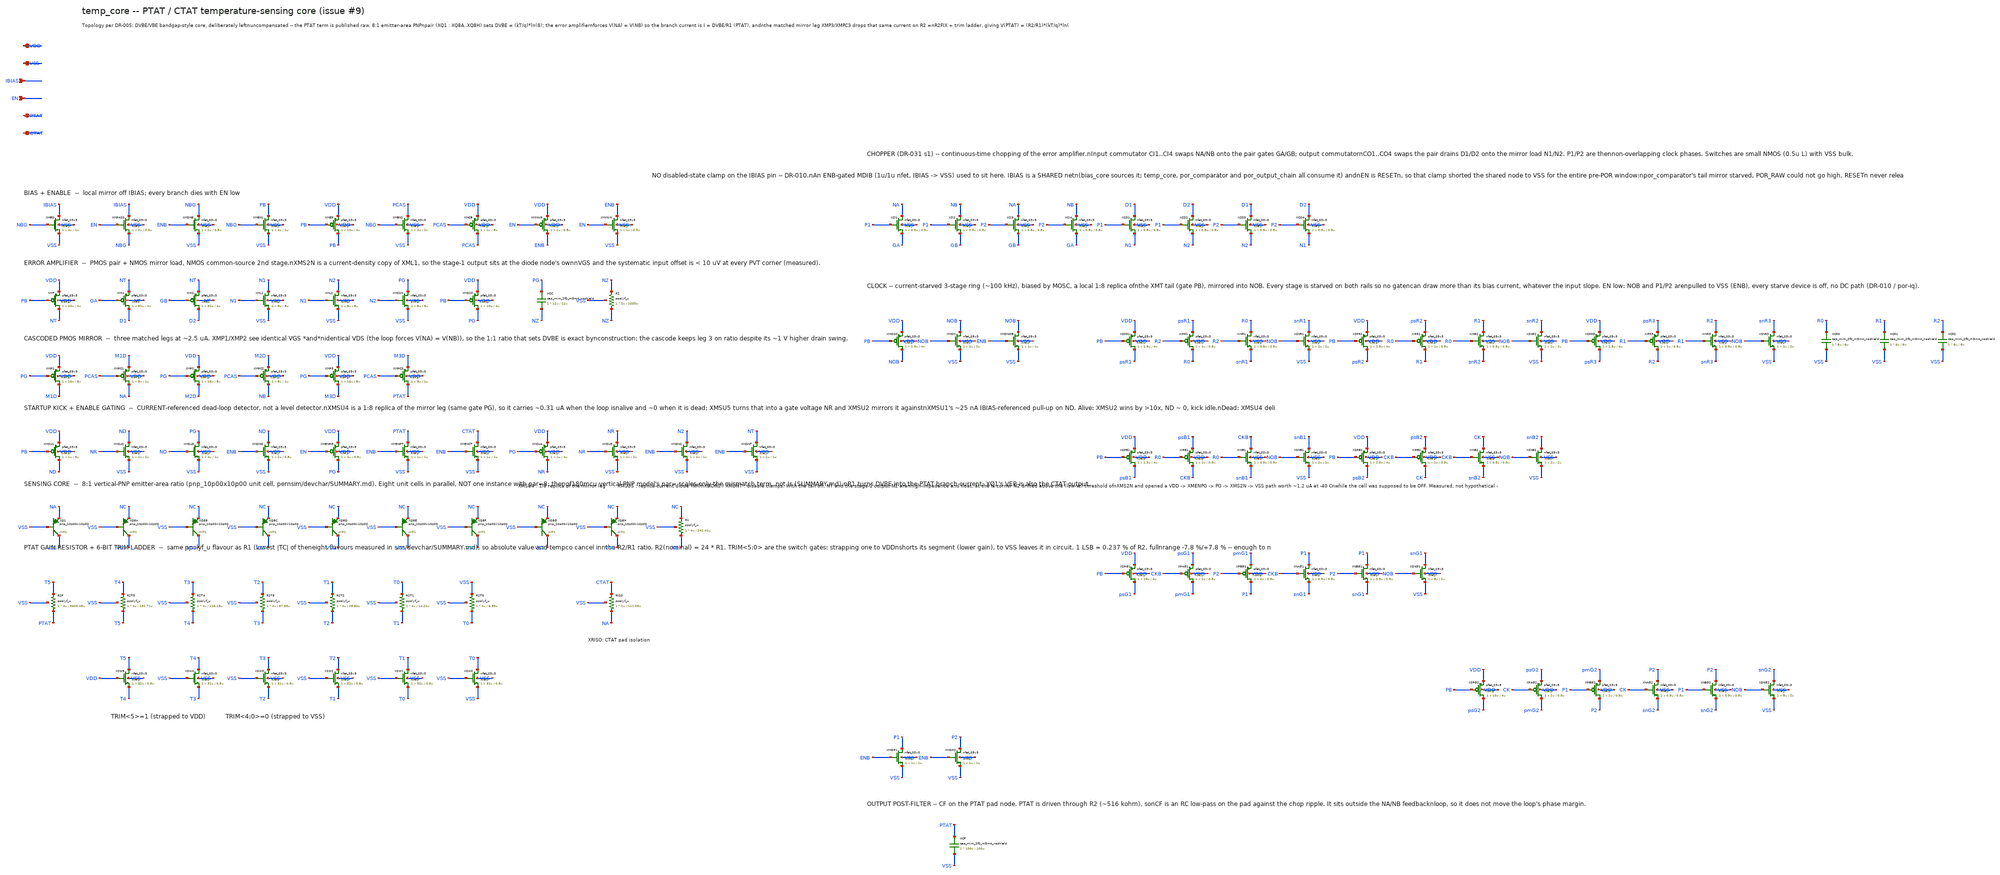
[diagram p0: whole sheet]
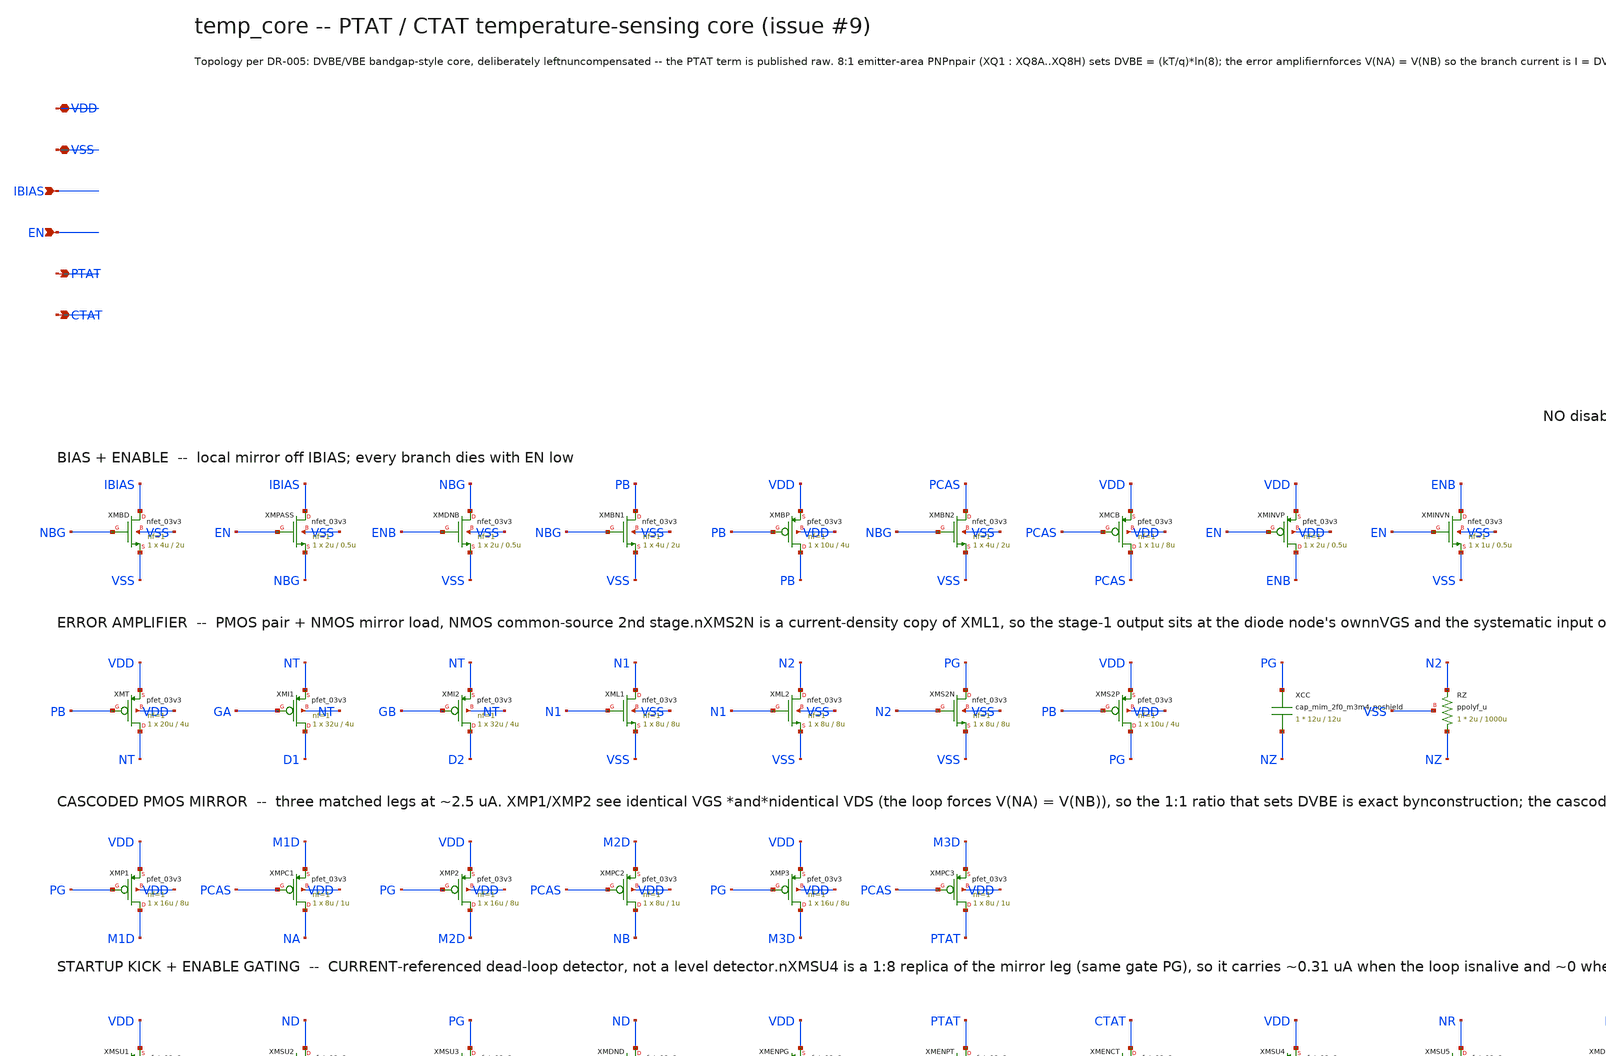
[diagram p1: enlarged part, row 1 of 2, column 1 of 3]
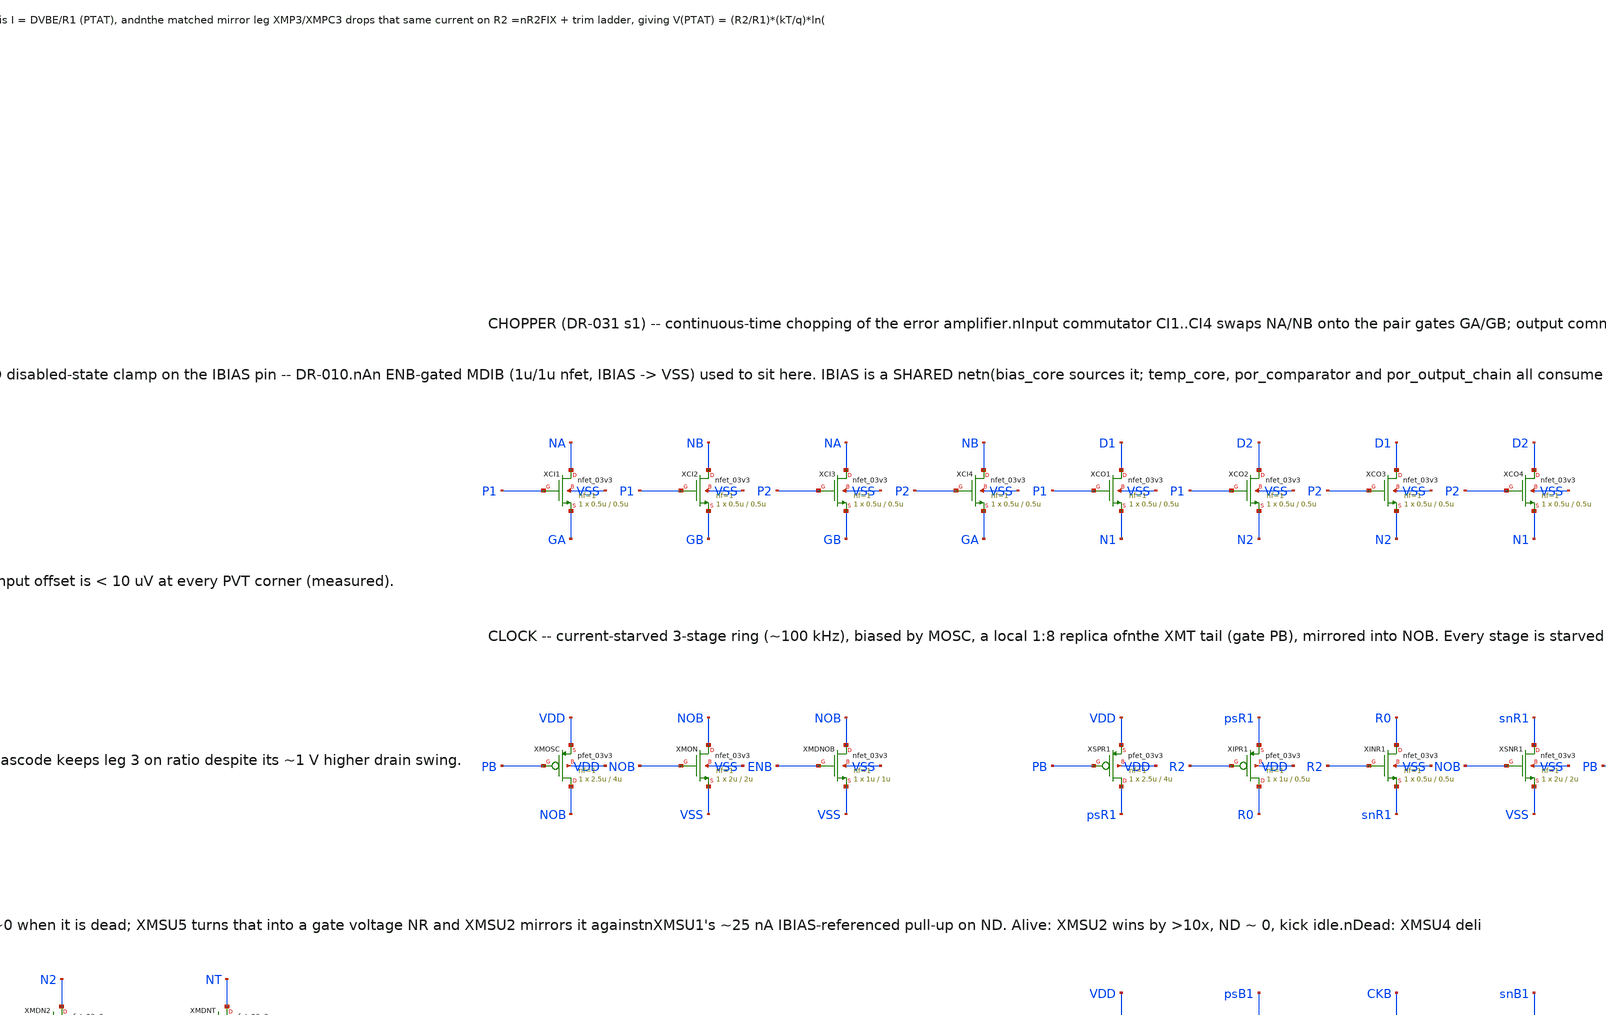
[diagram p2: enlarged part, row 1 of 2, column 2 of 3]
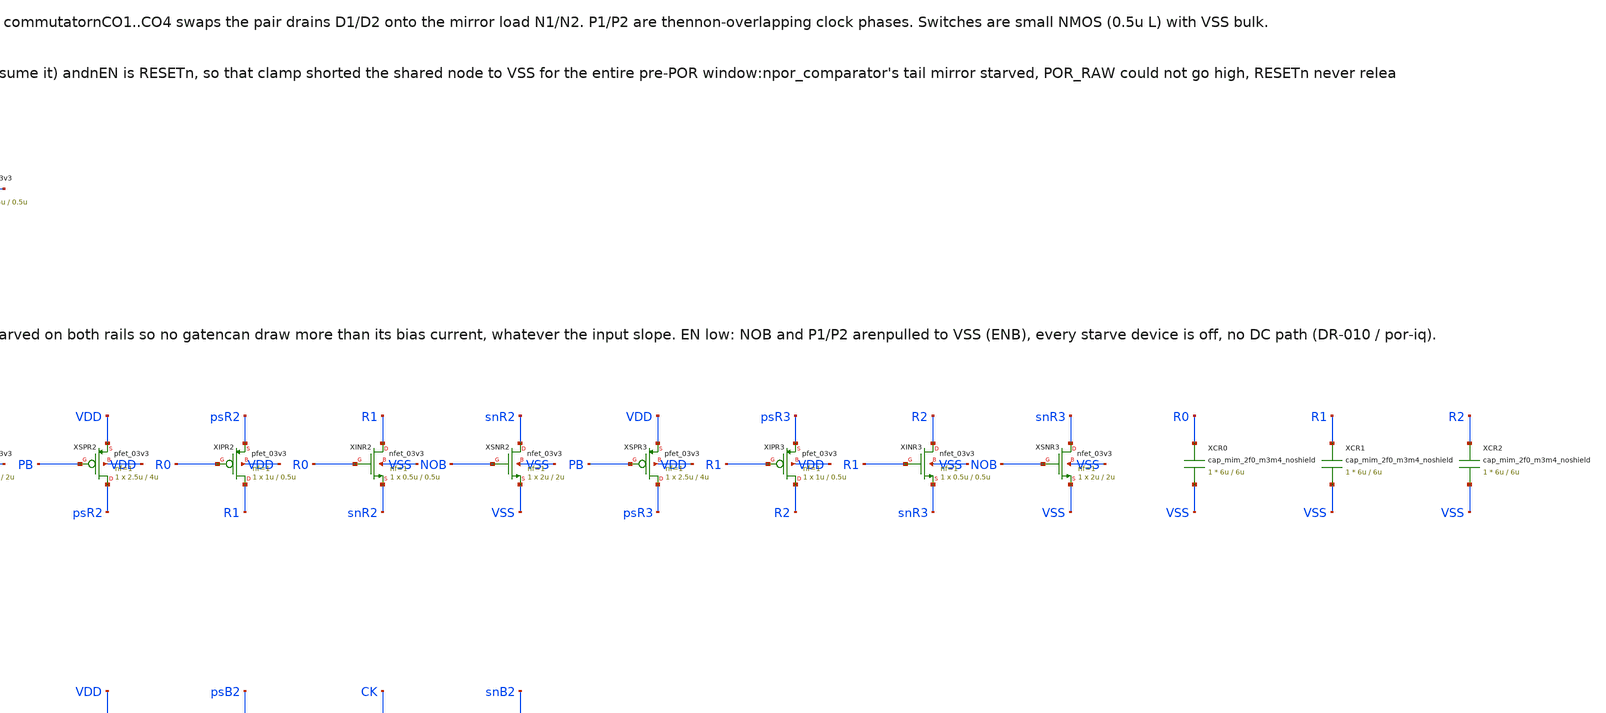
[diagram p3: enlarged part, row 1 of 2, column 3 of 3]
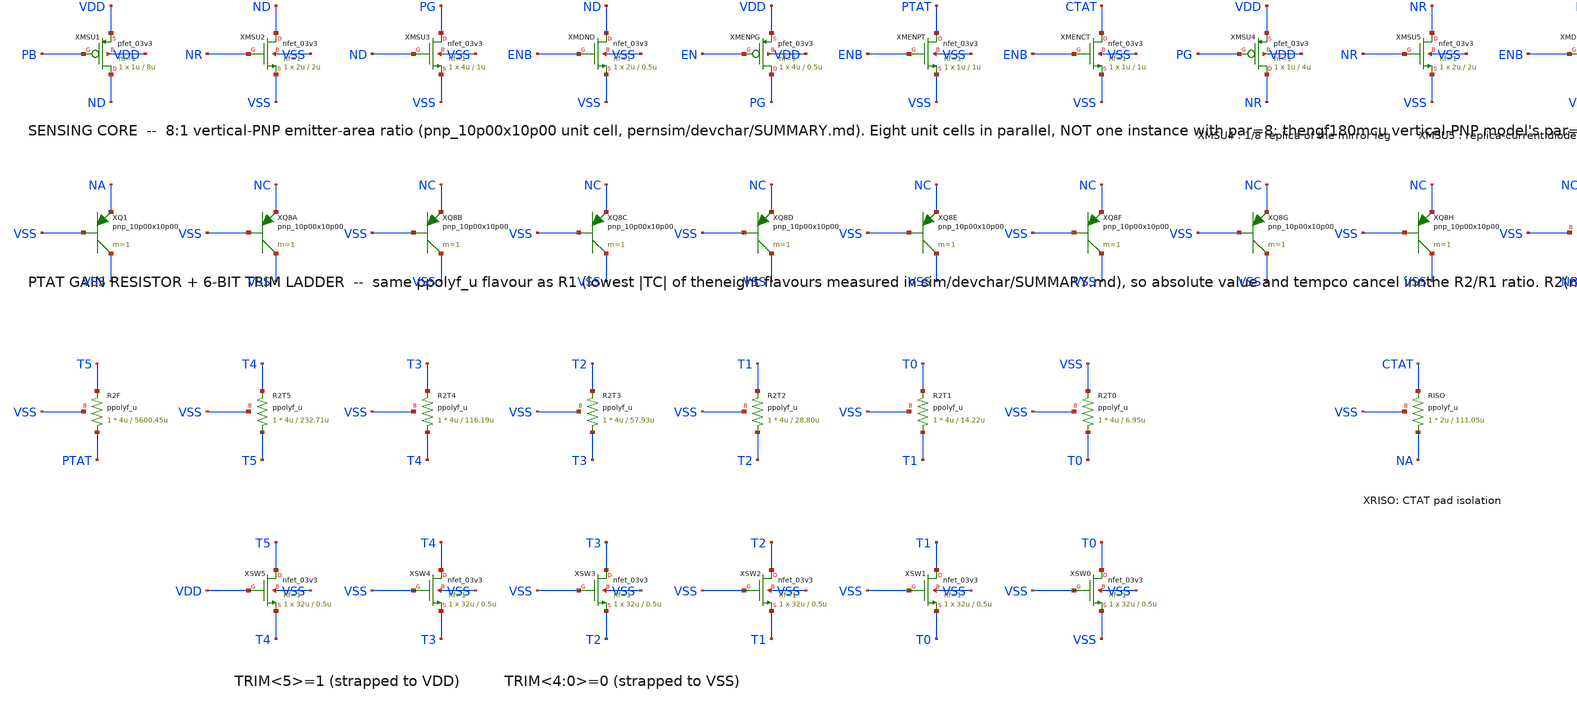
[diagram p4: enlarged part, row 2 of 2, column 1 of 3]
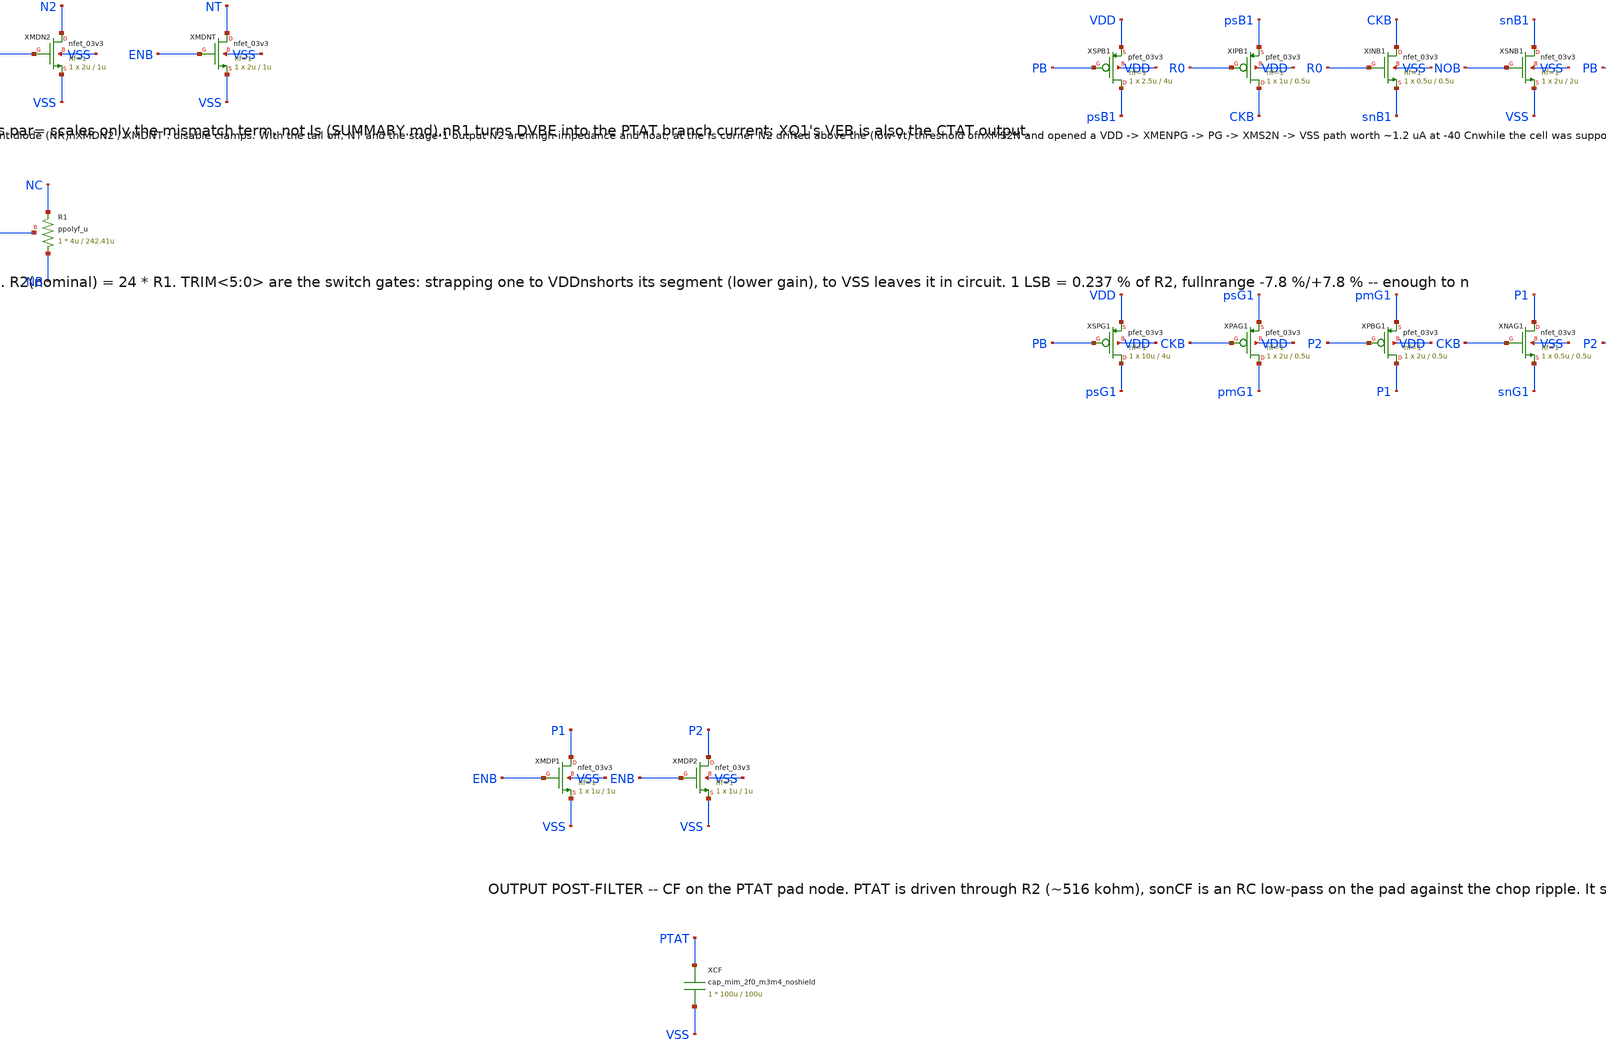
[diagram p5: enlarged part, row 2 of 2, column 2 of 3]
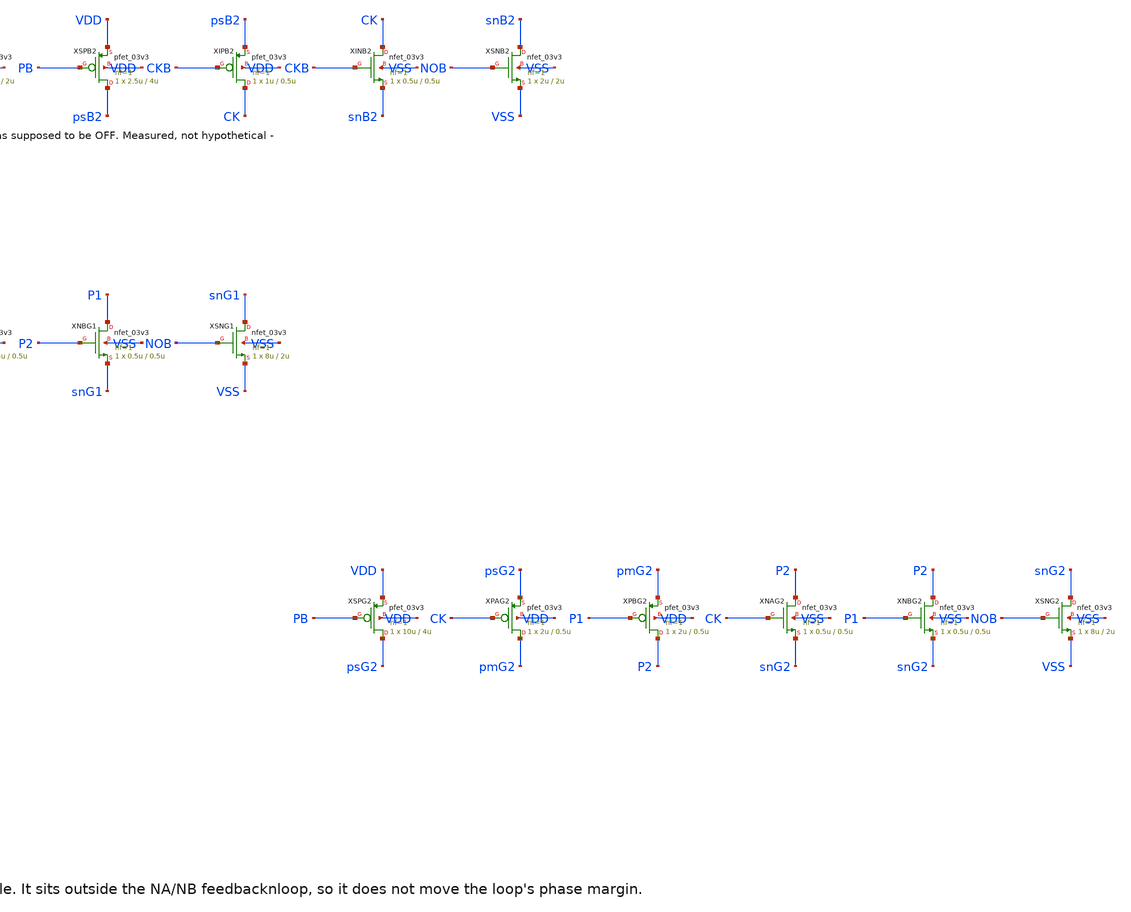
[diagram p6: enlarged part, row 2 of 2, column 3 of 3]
** sch_path: design/temp_core.sch
**.subckt temp_core VDD VSS IBIAS EN PTAT CTAT
*.iopin VDD
*.iopin VSS
*.ipin IBIAS
*.ipin EN
*.opin PTAT
*.opin CTAT
XMBD IBIAS NBG VSS VSS nfet_03v3 L=2u W=4u nf=1 ad='int((nf+1)/2) * W/nf * 0.18u' as='int((nf+2)/2) * W/nf * 0.18u'
+ pd='2*int((nf+1)/2) * (W/nf + 0.18u)' ps='2*int((nf+2)/2) * (W/nf + 0.18u)' nrd='0.18u / W' nrs='0.18u / W'
+ sa=0 sb=0 sd=0 m=1
XMPASS IBIAS EN NBG VSS nfet_03v3 L=0.5u W=2u nf=1 ad='int((nf+1)/2) * W/nf * 0.18u' as='int((nf+2)/2) * W/nf * 0.18u'
+ pd='2*int((nf+1)/2) * (W/nf + 0.18u)' ps='2*int((nf+2)/2) * (W/nf + 0.18u)' nrd='0.18u / W' nrs='0.18u / W'
+ sa=0 sb=0 sd=0 m=1
XMDNB NBG ENB VSS VSS nfet_03v3 L=0.5u W=2u nf=1 ad='int((nf+1)/2) * W/nf * 0.18u' as='int((nf+2)/2) * W/nf * 0.18u'
+ pd='2*int((nf+1)/2) * (W/nf + 0.18u)' ps='2*int((nf+2)/2) * (W/nf + 0.18u)' nrd='0.18u / W' nrs='0.18u / W'
+ sa=0 sb=0 sd=0 m=1
XMBN1 PB NBG VSS VSS nfet_03v3 L=2u W=4u nf=1 ad='int((nf+1)/2) * W/nf * 0.18u' as='int((nf+2)/2) * W/nf * 0.18u'
+ pd='2*int((nf+1)/2) * (W/nf + 0.18u)' ps='2*int((nf+2)/2) * (W/nf + 0.18u)' nrd='0.18u / W' nrs='0.18u / W'
+ sa=0 sb=0 sd=0 m=1
XMBP PB PB VDD VDD pfet_03v3 L=4u W=10u nf=1 ad='int((nf+1)/2) * W/nf * 0.18u' as='int((nf+2)/2) * W/nf * 0.18u'
+ pd='2*int((nf+1)/2) * (W/nf + 0.18u)' ps='2*int((nf+2)/2) * (W/nf + 0.18u)' nrd='0.18u / W' nrs='0.18u / W'
+ sa=0 sb=0 sd=0 m=1
XMBN2 PCAS NBG VSS VSS nfet_03v3 L=2u W=4u nf=1 ad='int((nf+1)/2) * W/nf * 0.18u' as='int((nf+2)/2) * W/nf * 0.18u'
+ pd='2*int((nf+1)/2) * (W/nf + 0.18u)' ps='2*int((nf+2)/2) * (W/nf + 0.18u)' nrd='0.18u / W' nrs='0.18u / W'
+ sa=0 sb=0 sd=0 m=1
XMCB PCAS PCAS VDD VDD pfet_03v3 L=8u W=1u nf=1 ad='int((nf+1)/2) * W/nf * 0.18u' as='int((nf+2)/2) * W/nf * 0.18u'
+ pd='2*int((nf+1)/2) * (W/nf + 0.18u)' ps='2*int((nf+2)/2) * (W/nf + 0.18u)' nrd='0.18u / W' nrs='0.18u / W'
+ sa=0 sb=0 sd=0 m=1
XMINVP ENB EN VDD VDD pfet_03v3 L=0.5u W=2u nf=1 ad='int((nf+1)/2) * W/nf * 0.18u' as='int((nf+2)/2) * W/nf * 0.18u'
+ pd='2*int((nf+1)/2) * (W/nf + 0.18u)' ps='2*int((nf+2)/2) * (W/nf + 0.18u)' nrd='0.18u / W' nrs='0.18u / W'
+ sa=0 sb=0 sd=0 m=1
XMINVN ENB EN VSS VSS nfet_03v3 L=0.5u W=1u nf=1 ad='int((nf+1)/2) * W/nf * 0.18u' as='int((nf+2)/2) * W/nf * 0.18u'
+ pd='2*int((nf+1)/2) * (W/nf + 0.18u)' ps='2*int((nf+2)/2) * (W/nf + 0.18u)' nrd='0.18u / W' nrs='0.18u / W'
+ sa=0 sb=0 sd=0 m=1
XMT NT PB VDD VDD pfet_03v3 L=4u W=20u nf=1 ad='int((nf+1)/2) * W/nf * 0.18u' as='int((nf+2)/2) * W/nf * 0.18u'
+ pd='2*int((nf+1)/2) * (W/nf + 0.18u)' ps='2*int((nf+2)/2) * (W/nf + 0.18u)' nrd='0.18u / W' nrs='0.18u / W'
+ sa=0 sb=0 sd=0 m=1
XMI1 D1 GA NT NT pfet_03v3 L=4u W=32u nf=1 ad='int((nf+1)/2) * W/nf * 0.18u' as='int((nf+2)/2) * W/nf * 0.18u'
+ pd='2*int((nf+1)/2) * (W/nf + 0.18u)' ps='2*int((nf+2)/2) * (W/nf + 0.18u)' nrd='0.18u / W' nrs='0.18u / W'
+ sa=0 sb=0 sd=0 m=1
XMI2 D2 GB NT NT pfet_03v3 L=4u W=32u nf=1 ad='int((nf+1)/2) * W/nf * 0.18u' as='int((nf+2)/2) * W/nf * 0.18u'
+ pd='2*int((nf+1)/2) * (W/nf + 0.18u)' ps='2*int((nf+2)/2) * (W/nf + 0.18u)' nrd='0.18u / W' nrs='0.18u / W'
+ sa=0 sb=0 sd=0 m=1
XML1 N1 N1 VSS VSS nfet_03v3 L=8u W=8u nf=1 ad='int((nf+1)/2) * W/nf * 0.18u' as='int((nf+2)/2) * W/nf * 0.18u'
+ pd='2*int((nf+1)/2) * (W/nf + 0.18u)' ps='2*int((nf+2)/2) * (W/nf + 0.18u)' nrd='0.18u / W' nrs='0.18u / W'
+ sa=0 sb=0 sd=0 m=1
XML2 N2 N1 VSS VSS nfet_03v3 L=8u W=8u nf=1 ad='int((nf+1)/2) * W/nf * 0.18u' as='int((nf+2)/2) * W/nf * 0.18u'
+ pd='2*int((nf+1)/2) * (W/nf + 0.18u)' ps='2*int((nf+2)/2) * (W/nf + 0.18u)' nrd='0.18u / W' nrs='0.18u / W'
+ sa=0 sb=0 sd=0 m=1
XMS2N PG N2 VSS VSS nfet_03v3 L=8u W=8u nf=1 ad='int((nf+1)/2) * W/nf * 0.18u' as='int((nf+2)/2) * W/nf * 0.18u'
+ pd='2*int((nf+1)/2) * (W/nf + 0.18u)' ps='2*int((nf+2)/2) * (W/nf + 0.18u)' nrd='0.18u / W' nrs='0.18u / W'
+ sa=0 sb=0 sd=0 m=1
XMS2P PG PB VDD VDD pfet_03v3 L=4u W=10u nf=1 ad='int((nf+1)/2) * W/nf * 0.18u' as='int((nf+2)/2) * W/nf * 0.18u'
+ pd='2*int((nf+1)/2) * (W/nf + 0.18u)' ps='2*int((nf+2)/2) * (W/nf + 0.18u)' nrd='0.18u / W' nrs='0.18u / W'
+ sa=0 sb=0 sd=0 m=1
XCC PG NZ cap_mim_2f0_m3m4_noshield c_width=12u c_length=12u m=1
XRZ NZ N2 VSS ppolyf_u r_width=2u r_length=1000u m=1
XMP1 M1D PG VDD VDD pfet_03v3 L=8u W=16u nf=1 ad='int((nf+1)/2) * W/nf * 0.18u' as='int((nf+2)/2) * W/nf * 0.18u'
+ pd='2*int((nf+1)/2) * (W/nf + 0.18u)' ps='2*int((nf+2)/2) * (W/nf + 0.18u)' nrd='0.18u / W' nrs='0.18u / W'
+ sa=0 sb=0 sd=0 m=1
XMPC1 NA PCAS M1D VDD pfet_03v3 L=1u W=8u nf=1 ad='int((nf+1)/2) * W/nf * 0.18u' as='int((nf+2)/2) * W/nf * 0.18u'
+ pd='2*int((nf+1)/2) * (W/nf + 0.18u)' ps='2*int((nf+2)/2) * (W/nf + 0.18u)' nrd='0.18u / W' nrs='0.18u / W'
+ sa=0 sb=0 sd=0 m=1
XMP2 M2D PG VDD VDD pfet_03v3 L=8u W=16u nf=1 ad='int((nf+1)/2) * W/nf * 0.18u' as='int((nf+2)/2) * W/nf * 0.18u'
+ pd='2*int((nf+1)/2) * (W/nf + 0.18u)' ps='2*int((nf+2)/2) * (W/nf + 0.18u)' nrd='0.18u / W' nrs='0.18u / W'
+ sa=0 sb=0 sd=0 m=1
XMPC2 NB PCAS M2D VDD pfet_03v3 L=1u W=8u nf=1 ad='int((nf+1)/2) * W/nf * 0.18u' as='int((nf+2)/2) * W/nf * 0.18u'
+ pd='2*int((nf+1)/2) * (W/nf + 0.18u)' ps='2*int((nf+2)/2) * (W/nf + 0.18u)' nrd='0.18u / W' nrs='0.18u / W'
+ sa=0 sb=0 sd=0 m=1
XMP3 M3D PG VDD VDD pfet_03v3 L=8u W=16u nf=1 ad='int((nf+1)/2) * W/nf * 0.18u' as='int((nf+2)/2) * W/nf * 0.18u'
+ pd='2*int((nf+1)/2) * (W/nf + 0.18u)' ps='2*int((nf+2)/2) * (W/nf + 0.18u)' nrd='0.18u / W' nrs='0.18u / W'
+ sa=0 sb=0 sd=0 m=1
XMPC3 PTAT PCAS M3D VDD pfet_03v3 L=1u W=8u nf=1 ad='int((nf+1)/2) * W/nf * 0.18u' as='int((nf+2)/2) * W/nf * 0.18u'
+ pd='2*int((nf+1)/2) * (W/nf + 0.18u)' ps='2*int((nf+2)/2) * (W/nf + 0.18u)' nrd='0.18u / W' nrs='0.18u / W'
+ sa=0 sb=0 sd=0 m=1
XMSU1 ND PB VDD VDD pfet_03v3 L=8u W=1u nf=1 ad='int((nf+1)/2) * W/nf * 0.18u' as='int((nf+2)/2) * W/nf * 0.18u'
+ pd='2*int((nf+1)/2) * (W/nf + 0.18u)' ps='2*int((nf+2)/2) * (W/nf + 0.18u)' nrd='0.18u / W' nrs='0.18u / W'
+ sa=0 sb=0 sd=0 m=1
XMSU2 ND NR VSS VSS nfet_03v3 L=2u W=2u nf=1 ad='int((nf+1)/2) * W/nf * 0.18u' as='int((nf+2)/2) * W/nf * 0.18u'
+ pd='2*int((nf+1)/2) * (W/nf + 0.18u)' ps='2*int((nf+2)/2) * (W/nf + 0.18u)' nrd='0.18u / W' nrs='0.18u / W'
+ sa=0 sb=0 sd=0 m=1
XMSU3 PG ND VSS VSS nfet_03v3 L=1u W=4u nf=1 ad='int((nf+1)/2) * W/nf * 0.18u' as='int((nf+2)/2) * W/nf * 0.18u'
+ pd='2*int((nf+1)/2) * (W/nf + 0.18u)' ps='2*int((nf+2)/2) * (W/nf + 0.18u)' nrd='0.18u / W' nrs='0.18u / W'
+ sa=0 sb=0 sd=0 m=1
XMDND ND ENB VSS VSS nfet_03v3 L=0.5u W=2u nf=1 ad='int((nf+1)/2) * W/nf * 0.18u' as='int((nf+2)/2) * W/nf * 0.18u'
+ pd='2*int((nf+1)/2) * (W/nf + 0.18u)' ps='2*int((nf+2)/2) * (W/nf + 0.18u)' nrd='0.18u / W' nrs='0.18u / W'
+ sa=0 sb=0 sd=0 m=1
XMENPG PG EN VDD VDD pfet_03v3 L=0.5u W=4u nf=1 ad='int((nf+1)/2) * W/nf * 0.18u' as='int((nf+2)/2) * W/nf * 0.18u'
+ pd='2*int((nf+1)/2) * (W/nf + 0.18u)' ps='2*int((nf+2)/2) * (W/nf + 0.18u)' nrd='0.18u / W' nrs='0.18u / W'
+ sa=0 sb=0 sd=0 m=1
XMENPT PTAT ENB VSS VSS nfet_03v3 L=1u W=1u nf=1 ad='int((nf+1)/2) * W/nf * 0.18u' as='int((nf+2)/2) * W/nf * 0.18u'
+ pd='2*int((nf+1)/2) * (W/nf + 0.18u)' ps='2*int((nf+2)/2) * (W/nf + 0.18u)' nrd='0.18u / W' nrs='0.18u / W'
+ sa=0 sb=0 sd=0 m=1
XMENCT CTAT ENB VSS VSS nfet_03v3 L=1u W=1u nf=1 ad='int((nf+1)/2) * W/nf * 0.18u' as='int((nf+2)/2) * W/nf * 0.18u'
+ pd='2*int((nf+1)/2) * (W/nf + 0.18u)' ps='2*int((nf+2)/2) * (W/nf + 0.18u)' nrd='0.18u / W' nrs='0.18u / W'
+ sa=0 sb=0 sd=0 m=1
XMSU4 NR PG VDD VDD pfet_03v3 L=4u W=1u nf=1 ad='int((nf+1)/2) * W/nf * 0.18u' as='int((nf+2)/2) * W/nf * 0.18u'
+ pd='2*int((nf+1)/2) * (W/nf + 0.18u)' ps='2*int((nf+2)/2) * (W/nf + 0.18u)' nrd='0.18u / W' nrs='0.18u / W'
+ sa=0 sb=0 sd=0 m=1
XMSU5 NR NR VSS VSS nfet_03v3 L=2u W=2u nf=1 ad='int((nf+1)/2) * W/nf * 0.18u' as='int((nf+2)/2) * W/nf * 0.18u'
+ pd='2*int((nf+1)/2) * (W/nf + 0.18u)' ps='2*int((nf+2)/2) * (W/nf + 0.18u)' nrd='0.18u / W' nrs='0.18u / W'
+ sa=0 sb=0 sd=0 m=1
XMDN2 N2 ENB VSS VSS nfet_03v3 L=1u W=2u nf=1 ad='int((nf+1)/2) * W/nf * 0.18u' as='int((nf+2)/2) * W/nf * 0.18u'
+ pd='2*int((nf+1)/2) * (W/nf + 0.18u)' ps='2*int((nf+2)/2) * (W/nf + 0.18u)' nrd='0.18u / W' nrs='0.18u / W'
+ sa=0 sb=0 sd=0 m=1
XMDNT NT ENB VSS VSS nfet_03v3 L=1u W=2u nf=1 ad='int((nf+1)/2) * W/nf * 0.18u' as='int((nf+2)/2) * W/nf * 0.18u'
+ pd='2*int((nf+1)/2) * (W/nf + 0.18u)' ps='2*int((nf+2)/2) * (W/nf + 0.18u)' nrd='0.18u / W' nrs='0.18u / W'
+ sa=0 sb=0 sd=0 m=1
XQ1 VSS VSS NA pnp_10p00x10p00 m=1
XQ8A VSS VSS NC pnp_10p00x10p00 m=1
XQ8B VSS VSS NC pnp_10p00x10p00 m=1
XQ8C VSS VSS NC pnp_10p00x10p00 m=1
XQ8D VSS VSS NC pnp_10p00x10p00 m=1
XQ8E VSS VSS NC pnp_10p00x10p00 m=1
XQ8F VSS VSS NC pnp_10p00x10p00 m=1
XQ8G VSS VSS NC pnp_10p00x10p00 m=1
XQ8H VSS VSS NC pnp_10p00x10p00 m=1
XR1 NB NC VSS ppolyf_u r_width=4u r_length=242.41u m=1
XR2F PTAT T5 VSS ppolyf_u r_width=4u r_length=5600.45u m=1
XR2T5 T5 T4 VSS ppolyf_u r_width=4u r_length=232.71u m=1
XR2T4 T4 T3 VSS ppolyf_u r_width=4u r_length=116.19u m=1
XR2T3 T3 T2 VSS ppolyf_u r_width=4u r_length=57.93u m=1
XR2T2 T2 T1 VSS ppolyf_u r_width=4u r_length=28.80u m=1
XR2T1 T1 T0 VSS ppolyf_u r_width=4u r_length=14.22u m=1
XR2T0 T0 VSS VSS ppolyf_u r_width=4u r_length=6.95u m=1
XRISO NA CTAT VSS ppolyf_u r_width=2u r_length=111.05u m=1
XSW5 T5 VDD T4 VSS nfet_03v3 L=0.5u W=32u nf=1 ad='int((nf+1)/2) * W/nf * 0.18u' as='int((nf+2)/2) * W/nf * 0.18u'
+ pd='2*int((nf+1)/2) * (W/nf + 0.18u)' ps='2*int((nf+2)/2) * (W/nf + 0.18u)' nrd='0.18u / W' nrs='0.18u / W'
+ sa=0 sb=0 sd=0 m=1
XSW4 T4 VSS T3 VSS nfet_03v3 L=0.5u W=32u nf=1 ad='int((nf+1)/2) * W/nf * 0.18u' as='int((nf+2)/2) * W/nf * 0.18u'
+ pd='2*int((nf+1)/2) * (W/nf + 0.18u)' ps='2*int((nf+2)/2) * (W/nf + 0.18u)' nrd='0.18u / W' nrs='0.18u / W'
+ sa=0 sb=0 sd=0 m=1
XSW3 T3 VSS T2 VSS nfet_03v3 L=0.5u W=32u nf=1 ad='int((nf+1)/2) * W/nf * 0.18u' as='int((nf+2)/2) * W/nf * 0.18u'
+ pd='2*int((nf+1)/2) * (W/nf + 0.18u)' ps='2*int((nf+2)/2) * (W/nf + 0.18u)' nrd='0.18u / W' nrs='0.18u / W'
+ sa=0 sb=0 sd=0 m=1
XSW2 T2 VSS T1 VSS nfet_03v3 L=0.5u W=32u nf=1 ad='int((nf+1)/2) * W/nf * 0.18u' as='int((nf+2)/2) * W/nf * 0.18u'
+ pd='2*int((nf+1)/2) * (W/nf + 0.18u)' ps='2*int((nf+2)/2) * (W/nf + 0.18u)' nrd='0.18u / W' nrs='0.18u / W'
+ sa=0 sb=0 sd=0 m=1
XSW1 T1 VSS T0 VSS nfet_03v3 L=0.5u W=32u nf=1 ad='int((nf+1)/2) * W/nf * 0.18u' as='int((nf+2)/2) * W/nf * 0.18u'
+ pd='2*int((nf+1)/2) * (W/nf + 0.18u)' ps='2*int((nf+2)/2) * (W/nf + 0.18u)' nrd='0.18u / W' nrs='0.18u / W'
+ sa=0 sb=0 sd=0 m=1
XSW0 T0 VSS VSS VSS nfet_03v3 L=0.5u W=32u nf=1 ad='int((nf+1)/2) * W/nf * 0.18u' as='int((nf+2)/2) * W/nf * 0.18u'
+ pd='2*int((nf+1)/2) * (W/nf + 0.18u)' ps='2*int((nf+2)/2) * (W/nf + 0.18u)' nrd='0.18u / W' nrs='0.18u / W'
+ sa=0 sb=0 sd=0 m=1
XCI1 NA P1 GA VSS nfet_03v3 L=0.5u W=0.5u nf=1 ad='int((nf+1)/2) * W/nf * 0.18u' as='int((nf+2)/2) * W/nf * 0.18u'
+ pd='2*int((nf+1)/2) * (W/nf + 0.18u)' ps='2*int((nf+2)/2) * (W/nf + 0.18u)' nrd='0.18u / W' nrs='0.18u / W'
+ sa=0 sb=0 sd=0 m=1
XCI2 NB P1 GB VSS nfet_03v3 L=0.5u W=0.5u nf=1 ad='int((nf+1)/2) * W/nf * 0.18u' as='int((nf+2)/2) * W/nf * 0.18u'
+ pd='2*int((nf+1)/2) * (W/nf + 0.18u)' ps='2*int((nf+2)/2) * (W/nf + 0.18u)' nrd='0.18u / W' nrs='0.18u / W'
+ sa=0 sb=0 sd=0 m=1
XCI3 NA P2 GB VSS nfet_03v3 L=0.5u W=0.5u nf=1 ad='int((nf+1)/2) * W/nf * 0.18u' as='int((nf+2)/2) * W/nf * 0.18u'
+ pd='2*int((nf+1)/2) * (W/nf + 0.18u)' ps='2*int((nf+2)/2) * (W/nf + 0.18u)' nrd='0.18u / W' nrs='0.18u / W'
+ sa=0 sb=0 sd=0 m=1
XCI4 NB P2 GA VSS nfet_03v3 L=0.5u W=0.5u nf=1 ad='int((nf+1)/2) * W/nf * 0.18u' as='int((nf+2)/2) * W/nf * 0.18u'
+ pd='2*int((nf+1)/2) * (W/nf + 0.18u)' ps='2*int((nf+2)/2) * (W/nf + 0.18u)' nrd='0.18u / W' nrs='0.18u / W'
+ sa=0 sb=0 sd=0 m=1
XCO1 D1 P1 N1 VSS nfet_03v3 L=0.5u W=0.5u nf=1 ad='int((nf+1)/2) * W/nf * 0.18u' as='int((nf+2)/2) * W/nf * 0.18u'
+ pd='2*int((nf+1)/2) * (W/nf + 0.18u)' ps='2*int((nf+2)/2) * (W/nf + 0.18u)' nrd='0.18u / W' nrs='0.18u / W'
+ sa=0 sb=0 sd=0 m=1
XCO2 D2 P1 N2 VSS nfet_03v3 L=0.5u W=0.5u nf=1 ad='int((nf+1)/2) * W/nf * 0.18u' as='int((nf+2)/2) * W/nf * 0.18u'
+ pd='2*int((nf+1)/2) * (W/nf + 0.18u)' ps='2*int((nf+2)/2) * (W/nf + 0.18u)' nrd='0.18u / W' nrs='0.18u / W'
+ sa=0 sb=0 sd=0 m=1
XCO3 D1 P2 N2 VSS nfet_03v3 L=0.5u W=0.5u nf=1 ad='int((nf+1)/2) * W/nf * 0.18u' as='int((nf+2)/2) * W/nf * 0.18u'
+ pd='2*int((nf+1)/2) * (W/nf + 0.18u)' ps='2*int((nf+2)/2) * (W/nf + 0.18u)' nrd='0.18u / W' nrs='0.18u / W'
+ sa=0 sb=0 sd=0 m=1
XCO4 D2 P2 N1 VSS nfet_03v3 L=0.5u W=0.5u nf=1 ad='int((nf+1)/2) * W/nf * 0.18u' as='int((nf+2)/2) * W/nf * 0.18u'
+ pd='2*int((nf+1)/2) * (W/nf + 0.18u)' ps='2*int((nf+2)/2) * (W/nf + 0.18u)' nrd='0.18u / W' nrs='0.18u / W'
+ sa=0 sb=0 sd=0 m=1
XMOSC NOB PB VDD VDD pfet_03v3 L=4u W=2.5u nf=1 ad='int((nf+1)/2) * W/nf * 0.18u' as='int((nf+2)/2) * W/nf * 0.18u'
+ pd='2*int((nf+1)/2) * (W/nf + 0.18u)' ps='2*int((nf+2)/2) * (W/nf + 0.18u)' nrd='0.18u / W' nrs='0.18u / W'
+ sa=0 sb=0 sd=0 m=1
XMON NOB NOB VSS VSS nfet_03v3 L=2u W=2u nf=1 ad='int((nf+1)/2) * W/nf * 0.18u' as='int((nf+2)/2) * W/nf * 0.18u'
+ pd='2*int((nf+1)/2) * (W/nf + 0.18u)' ps='2*int((nf+2)/2) * (W/nf + 0.18u)' nrd='0.18u / W' nrs='0.18u / W'
+ sa=0 sb=0 sd=0 m=1
XMDNOB NOB ENB VSS VSS nfet_03v3 L=1u W=1u nf=1 ad='int((nf+1)/2) * W/nf * 0.18u' as='int((nf+2)/2) * W/nf * 0.18u'
+ pd='2*int((nf+1)/2) * (W/nf + 0.18u)' ps='2*int((nf+2)/2) * (W/nf + 0.18u)' nrd='0.18u / W' nrs='0.18u / W'
+ sa=0 sb=0 sd=0 m=1
XSPR1 psR1 PB VDD VDD pfet_03v3 L=4u W=2.5u nf=1 ad='int((nf+1)/2) * W/nf * 0.18u' as='int((nf+2)/2) * W/nf * 0.18u'
+ pd='2*int((nf+1)/2) * (W/nf + 0.18u)' ps='2*int((nf+2)/2) * (W/nf + 0.18u)' nrd='0.18u / W' nrs='0.18u / W'
+ sa=0 sb=0 sd=0 m=1
XIPR1 R0 R2 psR1 VDD pfet_03v3 L=0.5u W=1u nf=1 ad='int((nf+1)/2) * W/nf * 0.18u' as='int((nf+2)/2) * W/nf * 0.18u'
+ pd='2*int((nf+1)/2) * (W/nf + 0.18u)' ps='2*int((nf+2)/2) * (W/nf + 0.18u)' nrd='0.18u / W' nrs='0.18u / W'
+ sa=0 sb=0 sd=0 m=1
XINR1 R0 R2 snR1 VSS nfet_03v3 L=0.5u W=0.5u nf=1 ad='int((nf+1)/2) * W/nf * 0.18u' as='int((nf+2)/2) * W/nf * 0.18u'
+ pd='2*int((nf+1)/2) * (W/nf + 0.18u)' ps='2*int((nf+2)/2) * (W/nf + 0.18u)' nrd='0.18u / W' nrs='0.18u / W'
+ sa=0 sb=0 sd=0 m=1
XSNR1 snR1 NOB VSS VSS nfet_03v3 L=2u W=2u nf=1 ad='int((nf+1)/2) * W/nf * 0.18u' as='int((nf+2)/2) * W/nf * 0.18u'
+ pd='2*int((nf+1)/2) * (W/nf + 0.18u)' ps='2*int((nf+2)/2) * (W/nf + 0.18u)' nrd='0.18u / W' nrs='0.18u / W'
+ sa=0 sb=0 sd=0 m=1
XSPR2 psR2 PB VDD VDD pfet_03v3 L=4u W=2.5u nf=1 ad='int((nf+1)/2) * W/nf * 0.18u' as='int((nf+2)/2) * W/nf * 0.18u'
+ pd='2*int((nf+1)/2) * (W/nf + 0.18u)' ps='2*int((nf+2)/2) * (W/nf + 0.18u)' nrd='0.18u / W' nrs='0.18u / W'
+ sa=0 sb=0 sd=0 m=1
XIPR2 R1 R0 psR2 VDD pfet_03v3 L=0.5u W=1u nf=1 ad='int((nf+1)/2) * W/nf * 0.18u' as='int((nf+2)/2) * W/nf * 0.18u'
+ pd='2*int((nf+1)/2) * (W/nf + 0.18u)' ps='2*int((nf+2)/2) * (W/nf + 0.18u)' nrd='0.18u / W' nrs='0.18u / W'
+ sa=0 sb=0 sd=0 m=1
XINR2 R1 R0 snR2 VSS nfet_03v3 L=0.5u W=0.5u nf=1 ad='int((nf+1)/2) * W/nf * 0.18u' as='int((nf+2)/2) * W/nf * 0.18u'
+ pd='2*int((nf+1)/2) * (W/nf + 0.18u)' ps='2*int((nf+2)/2) * (W/nf + 0.18u)' nrd='0.18u / W' nrs='0.18u / W'
+ sa=0 sb=0 sd=0 m=1
XSNR2 snR2 NOB VSS VSS nfet_03v3 L=2u W=2u nf=1 ad='int((nf+1)/2) * W/nf * 0.18u' as='int((nf+2)/2) * W/nf * 0.18u'
+ pd='2*int((nf+1)/2) * (W/nf + 0.18u)' ps='2*int((nf+2)/2) * (W/nf + 0.18u)' nrd='0.18u / W' nrs='0.18u / W'
+ sa=0 sb=0 sd=0 m=1
XSPR3 psR3 PB VDD VDD pfet_03v3 L=4u W=2.5u nf=1 ad='int((nf+1)/2) * W/nf * 0.18u' as='int((nf+2)/2) * W/nf * 0.18u'
+ pd='2*int((nf+1)/2) * (W/nf + 0.18u)' ps='2*int((nf+2)/2) * (W/nf + 0.18u)' nrd='0.18u / W' nrs='0.18u / W'
+ sa=0 sb=0 sd=0 m=1
XIPR3 R2 R1 psR3 VDD pfet_03v3 L=0.5u W=1u nf=1 ad='int((nf+1)/2) * W/nf * 0.18u' as='int((nf+2)/2) * W/nf * 0.18u'
+ pd='2*int((nf+1)/2) * (W/nf + 0.18u)' ps='2*int((nf+2)/2) * (W/nf + 0.18u)' nrd='0.18u / W' nrs='0.18u / W'
+ sa=0 sb=0 sd=0 m=1
XINR3 R2 R1 snR3 VSS nfet_03v3 L=0.5u W=0.5u nf=1 ad='int((nf+1)/2) * W/nf * 0.18u' as='int((nf+2)/2) * W/nf * 0.18u'
+ pd='2*int((nf+1)/2) * (W/nf + 0.18u)' ps='2*int((nf+2)/2) * (W/nf + 0.18u)' nrd='0.18u / W' nrs='0.18u / W'
+ sa=0 sb=0 sd=0 m=1
XSNR3 snR3 NOB VSS VSS nfet_03v3 L=2u W=2u nf=1 ad='int((nf+1)/2) * W/nf * 0.18u' as='int((nf+2)/2) * W/nf * 0.18u'
+ pd='2*int((nf+1)/2) * (W/nf + 0.18u)' ps='2*int((nf+2)/2) * (W/nf + 0.18u)' nrd='0.18u / W' nrs='0.18u / W'
+ sa=0 sb=0 sd=0 m=1
XCR0 R0 VSS cap_mim_2f0_m3m4_noshield c_width=6u c_length=6u m=1
XCR1 R1 VSS cap_mim_2f0_m3m4_noshield c_width=6u c_length=6u m=1
XCR2 R2 VSS cap_mim_2f0_m3m4_noshield c_width=6u c_length=6u m=1
XSPB1 psB1 PB VDD VDD pfet_03v3 L=4u W=2.5u nf=1 ad='int((nf+1)/2) * W/nf * 0.18u' as='int((nf+2)/2) * W/nf * 0.18u'
+ pd='2*int((nf+1)/2) * (W/nf + 0.18u)' ps='2*int((nf+2)/2) * (W/nf + 0.18u)' nrd='0.18u / W' nrs='0.18u / W'
+ sa=0 sb=0 sd=0 m=1
XIPB1 CKB R0 psB1 VDD pfet_03v3 L=0.5u W=1u nf=1 ad='int((nf+1)/2) * W/nf * 0.18u' as='int((nf+2)/2) * W/nf * 0.18u'
+ pd='2*int((nf+1)/2) * (W/nf + 0.18u)' ps='2*int((nf+2)/2) * (W/nf + 0.18u)' nrd='0.18u / W' nrs='0.18u / W'
+ sa=0 sb=0 sd=0 m=1
XINB1 CKB R0 snB1 VSS nfet_03v3 L=0.5u W=0.5u nf=1 ad='int((nf+1)/2) * W/nf * 0.18u' as='int((nf+2)/2) * W/nf * 0.18u'
+ pd='2*int((nf+1)/2) * (W/nf + 0.18u)' ps='2*int((nf+2)/2) * (W/nf + 0.18u)' nrd='0.18u / W' nrs='0.18u / W'
+ sa=0 sb=0 sd=0 m=1
XSNB1 snB1 NOB VSS VSS nfet_03v3 L=2u W=2u nf=1 ad='int((nf+1)/2) * W/nf * 0.18u' as='int((nf+2)/2) * W/nf * 0.18u'
+ pd='2*int((nf+1)/2) * (W/nf + 0.18u)' ps='2*int((nf+2)/2) * (W/nf + 0.18u)' nrd='0.18u / W' nrs='0.18u / W'
+ sa=0 sb=0 sd=0 m=1
XSPB2 psB2 PB VDD VDD pfet_03v3 L=4u W=2.5u nf=1 ad='int((nf+1)/2) * W/nf * 0.18u' as='int((nf+2)/2) * W/nf * 0.18u'
+ pd='2*int((nf+1)/2) * (W/nf + 0.18u)' ps='2*int((nf+2)/2) * (W/nf + 0.18u)' nrd='0.18u / W' nrs='0.18u / W'
+ sa=0 sb=0 sd=0 m=1
XIPB2 CK CKB psB2 VDD pfet_03v3 L=0.5u W=1u nf=1 ad='int((nf+1)/2) * W/nf * 0.18u' as='int((nf+2)/2) * W/nf * 0.18u'
+ pd='2*int((nf+1)/2) * (W/nf + 0.18u)' ps='2*int((nf+2)/2) * (W/nf + 0.18u)' nrd='0.18u / W' nrs='0.18u / W'
+ sa=0 sb=0 sd=0 m=1
XINB2 CK CKB snB2 VSS nfet_03v3 L=0.5u W=0.5u nf=1 ad='int((nf+1)/2) * W/nf * 0.18u' as='int((nf+2)/2) * W/nf * 0.18u'
+ pd='2*int((nf+1)/2) * (W/nf + 0.18u)' ps='2*int((nf+2)/2) * (W/nf + 0.18u)' nrd='0.18u / W' nrs='0.18u / W'
+ sa=0 sb=0 sd=0 m=1
XSNB2 snB2 NOB VSS VSS nfet_03v3 L=2u W=2u nf=1 ad='int((nf+1)/2) * W/nf * 0.18u' as='int((nf+2)/2) * W/nf * 0.18u'
+ pd='2*int((nf+1)/2) * (W/nf + 0.18u)' ps='2*int((nf+2)/2) * (W/nf + 0.18u)' nrd='0.18u / W' nrs='0.18u / W'
+ sa=0 sb=0 sd=0 m=1
XSPG1 psG1 PB VDD VDD pfet_03v3 L=4u W=10u nf=1 ad='int((nf+1)/2) * W/nf * 0.18u' as='int((nf+2)/2) * W/nf * 0.18u'
+ pd='2*int((nf+1)/2) * (W/nf + 0.18u)' ps='2*int((nf+2)/2) * (W/nf + 0.18u)' nrd='0.18u / W' nrs='0.18u / W'
+ sa=0 sb=0 sd=0 m=1
XPAG1 pmG1 CKB psG1 VDD pfet_03v3 L=0.5u W=2u nf=1 ad='int((nf+1)/2) * W/nf * 0.18u' as='int((nf+2)/2) * W/nf * 0.18u'
+ pd='2*int((nf+1)/2) * (W/nf + 0.18u)' ps='2*int((nf+2)/2) * (W/nf + 0.18u)' nrd='0.18u / W' nrs='0.18u / W'
+ sa=0 sb=0 sd=0 m=1
XPBG1 P1 P2 pmG1 VDD pfet_03v3 L=0.5u W=2u nf=1 ad='int((nf+1)/2) * W/nf * 0.18u' as='int((nf+2)/2) * W/nf * 0.18u'
+ pd='2*int((nf+1)/2) * (W/nf + 0.18u)' ps='2*int((nf+2)/2) * (W/nf + 0.18u)' nrd='0.18u / W' nrs='0.18u / W'
+ sa=0 sb=0 sd=0 m=1
XNAG1 P1 CKB snG1 VSS nfet_03v3 L=0.5u W=0.5u nf=1 ad='int((nf+1)/2) * W/nf * 0.18u' as='int((nf+2)/2) * W/nf * 0.18u'
+ pd='2*int((nf+1)/2) * (W/nf + 0.18u)' ps='2*int((nf+2)/2) * (W/nf + 0.18u)' nrd='0.18u / W' nrs='0.18u / W'
+ sa=0 sb=0 sd=0 m=1
XNBG1 P1 P2 snG1 VSS nfet_03v3 L=0.5u W=0.5u nf=1 ad='int((nf+1)/2) * W/nf * 0.18u' as='int((nf+2)/2) * W/nf * 0.18u'
+ pd='2*int((nf+1)/2) * (W/nf + 0.18u)' ps='2*int((nf+2)/2) * (W/nf + 0.18u)' nrd='0.18u / W' nrs='0.18u / W'
+ sa=0 sb=0 sd=0 m=1
XSNG1 snG1 NOB VSS VSS nfet_03v3 L=2u W=8u nf=1 ad='int((nf+1)/2) * W/nf * 0.18u' as='int((nf+2)/2) * W/nf * 0.18u'
+ pd='2*int((nf+1)/2) * (W/nf + 0.18u)' ps='2*int((nf+2)/2) * (W/nf + 0.18u)' nrd='0.18u / W' nrs='0.18u / W'
+ sa=0 sb=0 sd=0 m=1
XSPG2 psG2 PB VDD VDD pfet_03v3 L=4u W=10u nf=1 ad='int((nf+1)/2) * W/nf * 0.18u' as='int((nf+2)/2) * W/nf * 0.18u'
+ pd='2*int((nf+1)/2) * (W/nf + 0.18u)' ps='2*int((nf+2)/2) * (W/nf + 0.18u)' nrd='0.18u / W' nrs='0.18u / W'
+ sa=0 sb=0 sd=0 m=1
XPAG2 pmG2 CK psG2 VDD pfet_03v3 L=0.5u W=2u nf=1 ad='int((nf+1)/2) * W/nf * 0.18u' as='int((nf+2)/2) * W/nf * 0.18u'
+ pd='2*int((nf+1)/2) * (W/nf + 0.18u)' ps='2*int((nf+2)/2) * (W/nf + 0.18u)' nrd='0.18u / W' nrs='0.18u / W'
+ sa=0 sb=0 sd=0 m=1
XPBG2 P2 P1 pmG2 VDD pfet_03v3 L=0.5u W=2u nf=1 ad='int((nf+1)/2) * W/nf * 0.18u' as='int((nf+2)/2) * W/nf * 0.18u'
+ pd='2*int((nf+1)/2) * (W/nf + 0.18u)' ps='2*int((nf+2)/2) * (W/nf + 0.18u)' nrd='0.18u / W' nrs='0.18u / W'
+ sa=0 sb=0 sd=0 m=1
XNAG2 P2 CK snG2 VSS nfet_03v3 L=0.5u W=0.5u nf=1 ad='int((nf+1)/2) * W/nf * 0.18u' as='int((nf+2)/2) * W/nf * 0.18u'
+ pd='2*int((nf+1)/2) * (W/nf + 0.18u)' ps='2*int((nf+2)/2) * (W/nf + 0.18u)' nrd='0.18u / W' nrs='0.18u / W'
+ sa=0 sb=0 sd=0 m=1
XNBG2 P2 P1 snG2 VSS nfet_03v3 L=0.5u W=0.5u nf=1 ad='int((nf+1)/2) * W/nf * 0.18u' as='int((nf+2)/2) * W/nf * 0.18u'
+ pd='2*int((nf+1)/2) * (W/nf + 0.18u)' ps='2*int((nf+2)/2) * (W/nf + 0.18u)' nrd='0.18u / W' nrs='0.18u / W'
+ sa=0 sb=0 sd=0 m=1
XSNG2 snG2 NOB VSS VSS nfet_03v3 L=2u W=8u nf=1 ad='int((nf+1)/2) * W/nf * 0.18u' as='int((nf+2)/2) * W/nf * 0.18u'
+ pd='2*int((nf+1)/2) * (W/nf + 0.18u)' ps='2*int((nf+2)/2) * (W/nf + 0.18u)' nrd='0.18u / W' nrs='0.18u / W'
+ sa=0 sb=0 sd=0 m=1
XMDP1 P1 ENB VSS VSS nfet_03v3 L=1u W=1u nf=1 ad='int((nf+1)/2) * W/nf * 0.18u' as='int((nf+2)/2) * W/nf * 0.18u'
+ pd='2*int((nf+1)/2) * (W/nf + 0.18u)' ps='2*int((nf+2)/2) * (W/nf + 0.18u)' nrd='0.18u / W' nrs='0.18u / W'
+ sa=0 sb=0 sd=0 m=1
XMDP2 P2 ENB VSS VSS nfet_03v3 L=1u W=1u nf=1 ad='int((nf+1)/2) * W/nf * 0.18u' as='int((nf+2)/2) * W/nf * 0.18u'
+ pd='2*int((nf+1)/2) * (W/nf + 0.18u)' ps='2*int((nf+2)/2) * (W/nf + 0.18u)' nrd='0.18u / W' nrs='0.18u / W'
+ sa=0 sb=0 sd=0 m=1
XCF PTAT VSS cap_mim_2f0_m3m4_noshield c_width=100u c_length=100u m=1
**.ends
.end
